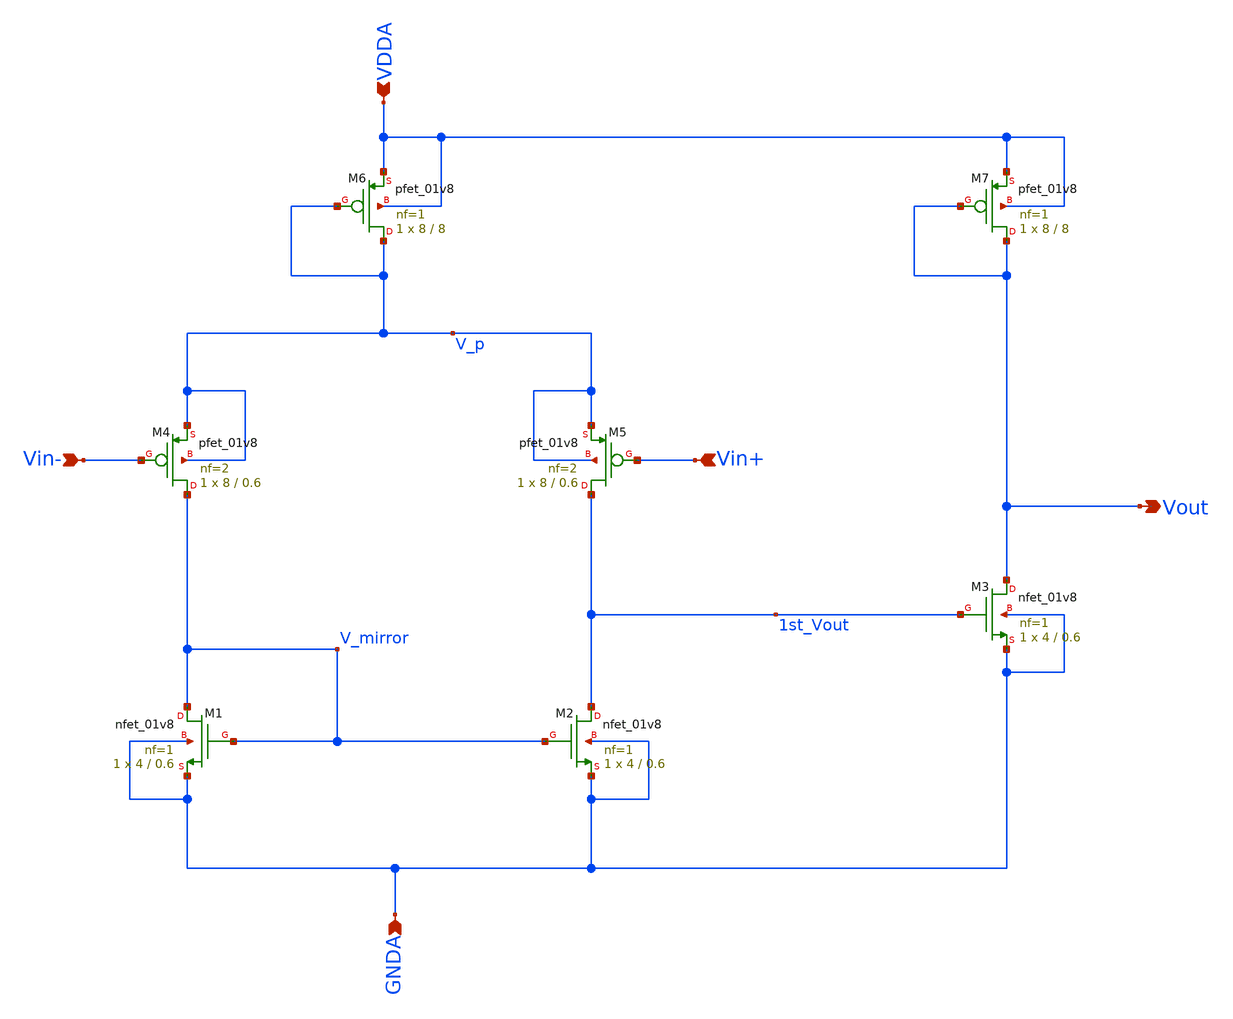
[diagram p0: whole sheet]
** sch_path: projects/bandgapref/xschem_ngspice/new_files/opamp_bandgap_3.sch
**.subckt opamp_bandgap_3 Vin+ Vout Vin- GNDA VDDA
*.ipin Vin+
*.opin Vout
*.ipin Vin-
*.ipin GNDA
*.ipin VDDA
XM1 V_mirror V_mirror GNDA GNDA sky130_fd_pr__nfet_01v8 L=0.6 W=4 nf=1 ad='int((nf+1)/2) * W/nf * 0.29'
+ as='int((nf+2)/2) * W/nf * 0.29' pd='2*int((nf+1)/2) * (W/nf + 0.29)' ps='2*int((nf+2)/2) * (W/nf + 0.29)'
+ nrd='0.29 / W' nrs='0.29 / W' sa=0 sb=0 sd=0 mult=1 m=1
XM2 1st_Vout V_mirror GNDA GNDA sky130_fd_pr__nfet_01v8 L=0.6 W=4 nf=1 ad='int((nf+1)/2) * W/nf * 0.29'
+ as='int((nf+2)/2) * W/nf * 0.29' pd='2*int((nf+1)/2) * (W/nf + 0.29)' ps='2*int((nf+2)/2) * (W/nf + 0.29)'
+ nrd='0.29 / W' nrs='0.29 / W' sa=0 sb=0 sd=0 mult=1 m=1
XM4 V_mirror Vin- V_p V_p sky130_fd_pr__pfet_01v8 L=0.6 W=8 nf=2 ad='int((nf+1)/2) * W/nf * 0.29' as='int((nf+2)/2) * W/nf * 0.29'
+ pd='2*int((nf+1)/2) * (W/nf + 0.29)' ps='2*int((nf+2)/2) * (W/nf + 0.29)' nrd='0.29 / W' nrs='0.29 / W'
+ sa=0 sb=0 sd=0 mult=1 m=1
XM5 1st_Vout Vin+ V_p V_p sky130_fd_pr__pfet_01v8 L=0.6 W=8 nf=2 ad='int((nf+1)/2) * W/nf * 0.29' as='int((nf+2)/2) * W/nf * 0.29'
+ pd='2*int((nf+1)/2) * (W/nf + 0.29)' ps='2*int((nf+2)/2) * (W/nf + 0.29)' nrd='0.29 / W' nrs='0.29 / W'
+ sa=0 sb=0 sd=0 mult=1 m=1
XM6 V_p V_p VDDA VDDA sky130_fd_pr__pfet_01v8 L=8 W=8 nf=1 ad='int((nf+1)/2) * W/nf * 0.29' as='int((nf+2)/2) * W/nf * 0.29'
+ pd='2*int((nf+1)/2) * (W/nf + 0.29)' ps='2*int((nf+2)/2) * (W/nf + 0.29)' nrd='0.29 / W' nrs='0.29 / W'
+ sa=0 sb=0 sd=0 mult=1 m=1
XM3 Vout 1st_Vout GNDA GNDA sky130_fd_pr__nfet_01v8 L=0.6 W=4 nf=1 ad='int((nf+1)/2) * W/nf * 0.29' as='int((nf+2)/2) * W/nf * 0.29'
+ pd='2*int((nf+1)/2) * (W/nf + 0.29)' ps='2*int((nf+2)/2) * (W/nf + 0.29)' nrd='0.29 / W' nrs='0.29 / W'
+ sa=0 sb=0 sd=0 mult=1 m=1
XM7 Vout Vout VDDA VDDA sky130_fd_pr__pfet_01v8 L=8 W=8 nf=1 ad='int((nf+1)/2) * W/nf * 0.29' as='int((nf+2)/2) * W/nf * 0.29'
+ pd='2*int((nf+1)/2) * (W/nf + 0.29)' ps='2*int((nf+2)/2) * (W/nf + 0.29)' nrd='0.29 / W' nrs='0.29 / W'
+ sa=0 sb=0 sd=0 mult=1 m=1
**.ends
.end
